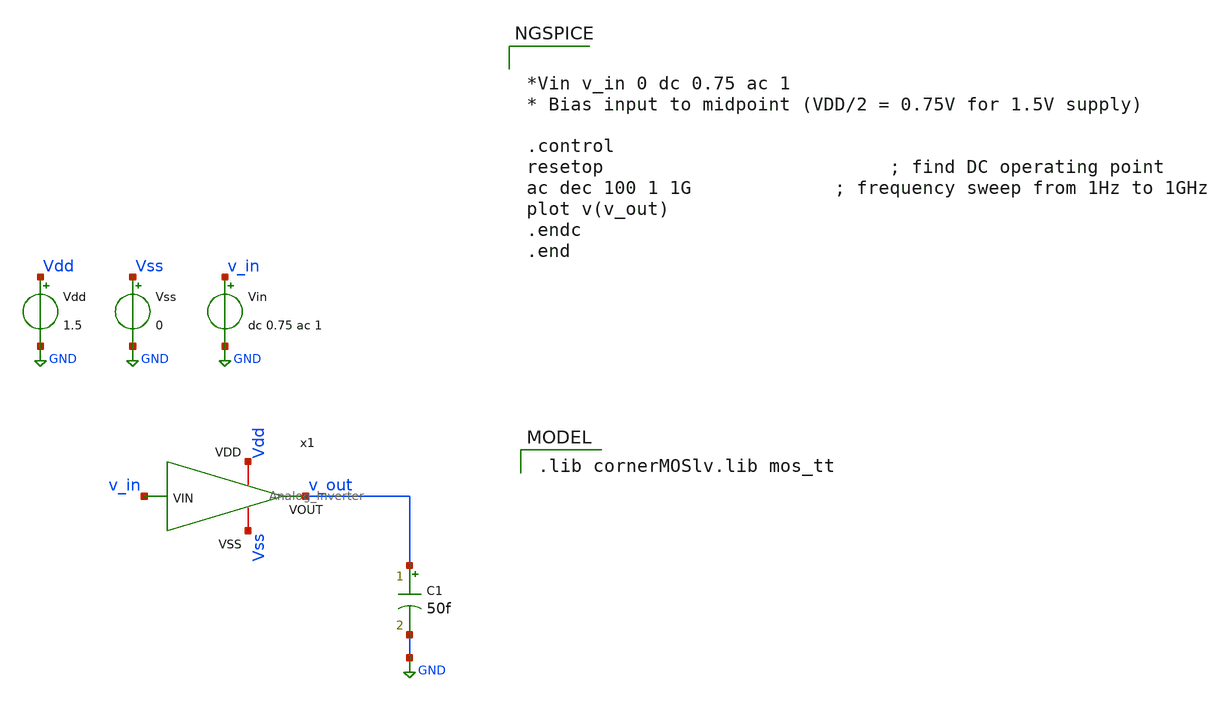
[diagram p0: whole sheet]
** sch_path: files/Analog_Inverter/1_schematics/tb_Analog_Inverter_ac.sch
**.subckt tb_Analog_Inverter_ac
Vdd Vdd GND 1.5
Vss Vss GND 0
Vin v_in GND dc 0.75 ac 1
C1 v_out GND 50f m=1
x1 Vdd v_in v_out Vss Analog_Inverter
**** begin user architecture code


*Vin v_in 0 dc 0.75 ac 1
* Bias input to midpoint (VDD/2 = 0.75V for 1.5V supply)

.control
resetop                          ; find DC operating point
ac dec 100 1 1G             ; frequency sweep from 1Hz to 1GHz
plot v(v_out)
.endc
.end


 .lib cornerMOSlv.lib mos_tt

**** end user architecture code
**.ends
.GLOBAL GND
.end
